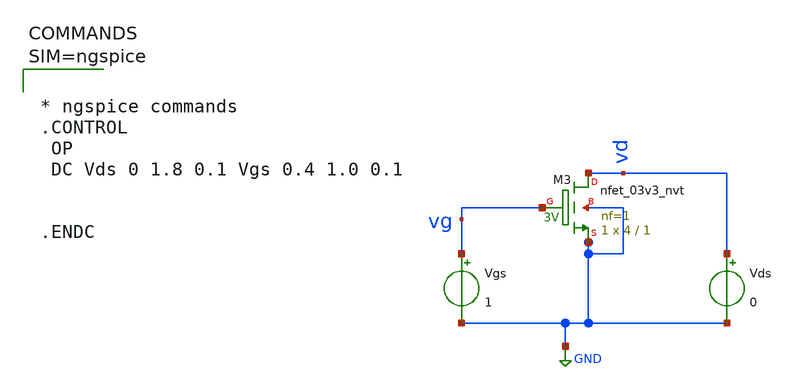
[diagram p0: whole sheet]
** sch_path: work/xschem/trans_nmos3.sch
**.subckt trans_nmos3
Vgs vg GND 1
Vds vd GND 0
XM3 vd vg GND GND sky130_fd_pr__nfet_03v3_nvt L=1 W=4 nf=1 ad='int((1 + 1)/2) * 4 / 1 * 0.29' as='int((1 + 2)/2) * 4 / 1 * 0.29'
+ pd='2*int((1 + 1)/2) * (4 / 1 + 0.29)' ps='2*int((1 + 2)/2) * (4 / 1 + 0.29)' nrd='0.29 / 4 ' nrs='0.29 / 4 '
+ sa=0 sb=0 sd=0 mult=1 m=1
**** begin user architecture code



* ngspice commands
.CONTROL
 OP
 DC Vds 0 1.8 0.1 Vgs 0.4 1.0 0.1


.ENDC




** opencircuitdesign pdks install
.lib $::SKYWATER_MODELS/sky130.lib.spice tt

**** end user architecture code
**.ends
.GLOBAL GND
.end
